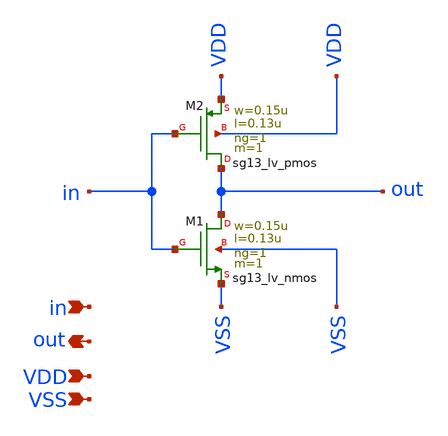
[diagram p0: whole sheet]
** sch_path: inverter.sch
**.subckt inverter in VDD VSS out
*.ipin in
*.ipin VDD
*.ipin VSS
*.opin out
XM1 out in VSS VSS sg13_lv_nmos w=0.15u l=0.13u ng=1 m=1 mm_ok=1
XM2 out in VDD VDD sg13_lv_pmos w=0.15u l=0.13u ng=1 m=1 mm_ok=1
**.ends
.end
